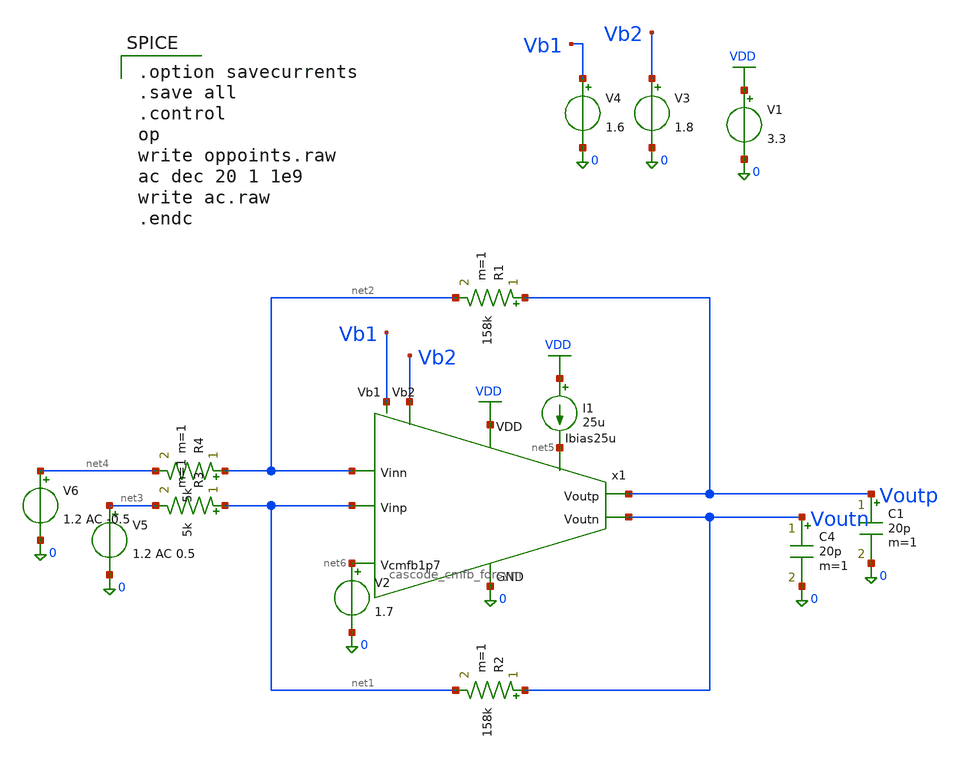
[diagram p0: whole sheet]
** sch_path: fda.sch
**.subckt fda
C4 Voutn 0 20p m=1
C1 Voutp 0 20p m=1
I1 VDD net5 25u
V1 VDD 0 3.3
V3 Vb2 0 1.8
V4 Vb1 0 1.6
V2 net6 0 1.7
x1 VDD Vb2 Voutp Voutn Vb1 net5 net2 net6 0 net1 cascode_cmfb_forsym
R1 Voutp net2 158k m=1
R2 Voutn net1 158k m=1
R3 net1 net3 5k m=1
R4 net2 net4 5k m=1
V5 net3 0 1.2 AC 0.5
V6 net4 0 1.2 AC -0.5
**** begin user architecture code

.option savecurrents
.save all
.control
op
write oppoints.raw
ac dec 20 1 1e9
write ac.raw
.endc


.include $::180MCU_MODELS/design.ngspice
.lib $::180MCU_MODELS/sm141064.ngspice typical
.lib $::180MCU_MODELS/smbb000149.ngspice typical

**** end user architecture code
**.ends
.GLOBAL VDD
.end
